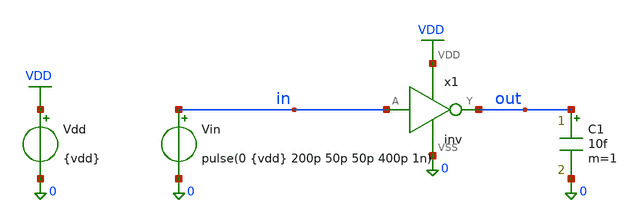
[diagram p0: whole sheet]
** sch_path: examples/ihp-inv/libs/cells/tb_inv/schematic/tb_inv.sch
**.subckt tb_inv
x1 in out VDD 0 inv
Vdd VDD 0 {vdd}
Vin in 0 pulse(0 {vdd} 200p 50p 50p 400p 1n)
C1 out 0 10f m=1
**.ends
.GLOBAL VDD
.end
